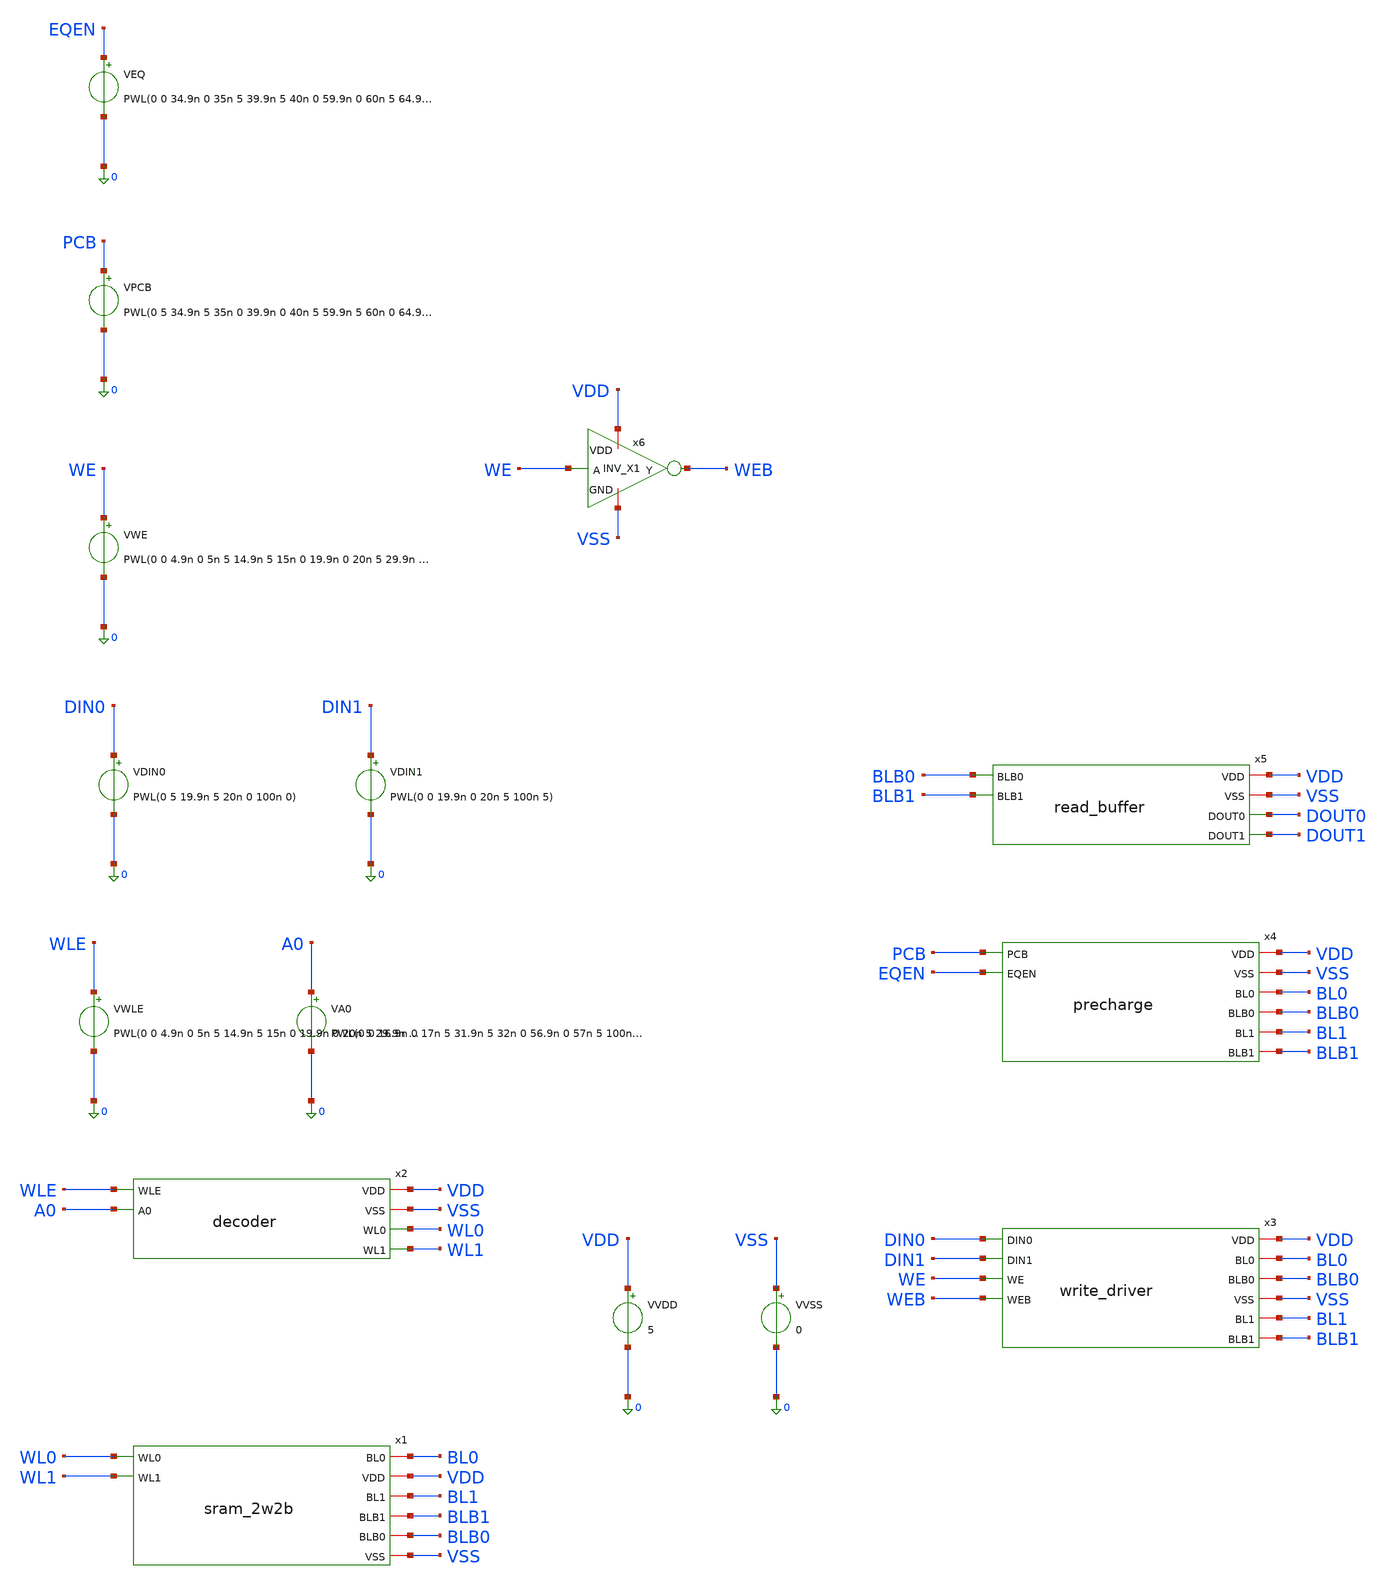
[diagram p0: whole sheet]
** sch_path: array/2word_x_2bit/tb_sram_2w2b_04.sch
**.subckt tb_sram_2w2b_04
x1 WL0 BL0 VDD BL1 BLB1 WL1 BLB0 VSS sram_2w2b
VVDD VDD 0 5
VDIN0 DIN0 0 PWL(0 5 19.9n 5 20n 0 100n 0)
VVSS VSS 0 0
VWE WE 0 PWL(0 0 4.9n 0 5n 5 14.9n 5 15n 0 19.9n 0 20n 5 29.9n 5 30n 0 100n 0)
VPCB PCB 0 PWL(0 5 34.9n 5 35n 0 39.9n 0 40n 5 59.9n 5 60n 0 64.9n 0 65n 5 100n 5)
VEQ EQEN 0 PWL(0 0 34.9n 0 35n 5 39.9n 5 40n 0 59.9n 0 60n 5 64.9n 5 65n 0 100n 0)
x2 VDD VSS WL0 WLE A0 WL1 decoder
VWLE WLE 0 PWL(0 0 4.9n 0 5n 5 14.9n 5 15n 0 19.9n 0 20n 5 29.9n 5 30n 0 44.9n 0 45n 5 54.9n 5 55n 0
+ 69.9n 0 70n 5 79.9n 5 80n 0 100n 0)
VA0 A0 0 PWL(0 0 16.9n 0 17n 5 31.9n 5 32n 0 56.9n 0 57n 5 100n 5)
x3 DIN0 VDD BL0 BLB0 VSS DIN1 BL1 WE BLB1 WEB write_driver
VDIN1 DIN1 0 PWL(0 0 19.9n 0 20n 5 100n 5)
x4 VDD VSS PCB EQEN BL0 BLB0 BL1 BLB1 precharge
x5 VDD VSS BLB0 BLB1 DOUT0 DOUT1 read_buffer
x6 VDD WE WEB VSS INV_X1
**** begin user architecture code
 .include $::LIB/ip62_models


.tran 10p 100n

.meas tran t_read0 TRIG v(wl0) VAL=2.5 RISE=2 TARG v(dout0) VAL=2.5 RISE=1 TD=40n
.meas tran t_read1 TRIG v(wl1) VAL=2.5 RISE=2 TARG v(dout1) VAL=2.5 RISE=1 TD=65n

.control
run
plot v(wl0) v(wl1)+6 v(dout0)+12 v(dout1)+18
.endc


**** end user architecture code
**.ends
.end
